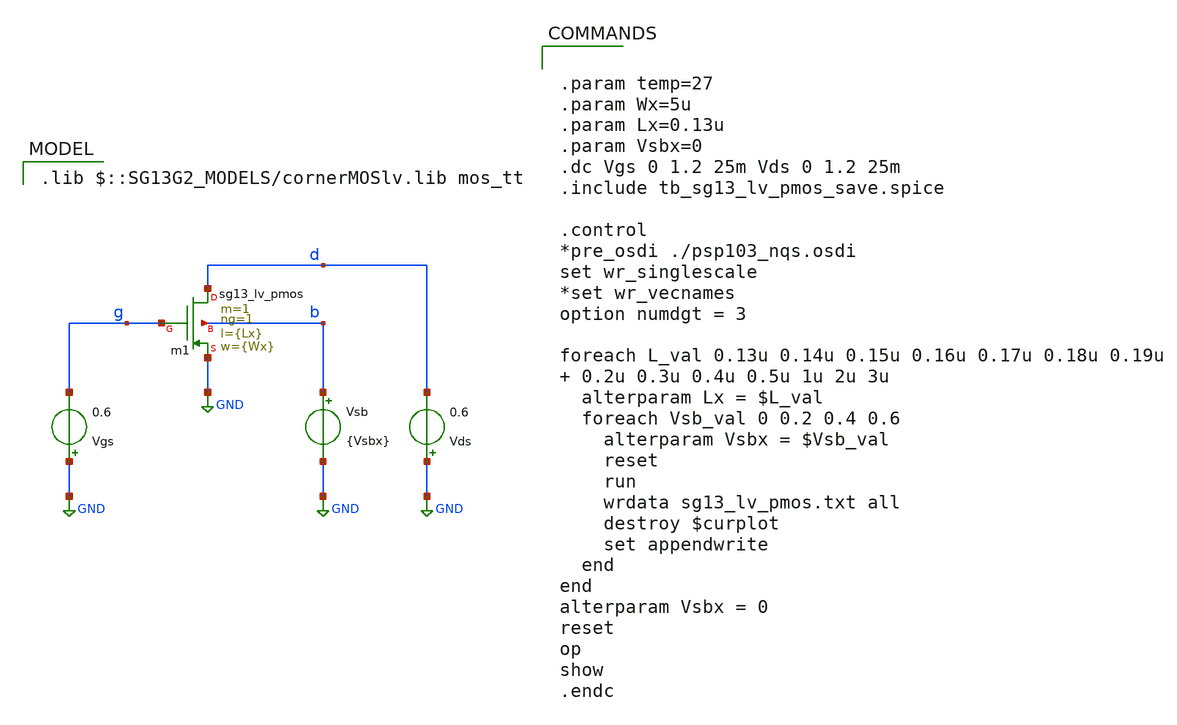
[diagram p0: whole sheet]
** sch_path: 4_Technology/src/tb_sg13_lv_pmos.sch
**.subckt tb_sg13_lv_pmos
Vgs GND g 0.6
Vds GND d 0.6
Vsb b GND {Vsbx}
Xm1 d g GND b sg13_lv_pmos w={Wx} l={Lx} ng=1 m=1 mm_ok=1
**** begin user architecture code
 .lib $::SG13G2_MODELS/cornerMOSlv.lib mos_tt



.param temp=27
.param Wx=5u
.param Lx=0.13u
.param Vsbx=0
.dc Vgs 0 1.2 25m Vds 0 1.2 25m
.include tb_sg13_lv_pmos_save.spice

.control
*pre_osdi ./psp103_nqs.osdi
set wr_singlescale
*set wr_vecnames
option numdgt = 3

foreach L_val 0.13u 0.14u 0.15u 0.16u 0.17u 0.18u 0.19u  0.2u 0.3u 0.4u 0.5u 1u 2u 3u
  alterparam Lx = $L_val
  foreach Vsb_val 0 0.2 0.4 0.6
    alterparam Vsbx = $Vsb_val
    reset
    run
    wrdata sg13_lv_pmos.txt all
    destroy $curplot
    set appendwrite
  end
end
alterparam Vsbx = 0
reset
op
show
.endc


**** end user architecture code
**.ends
.GLOBAL GND
.end
